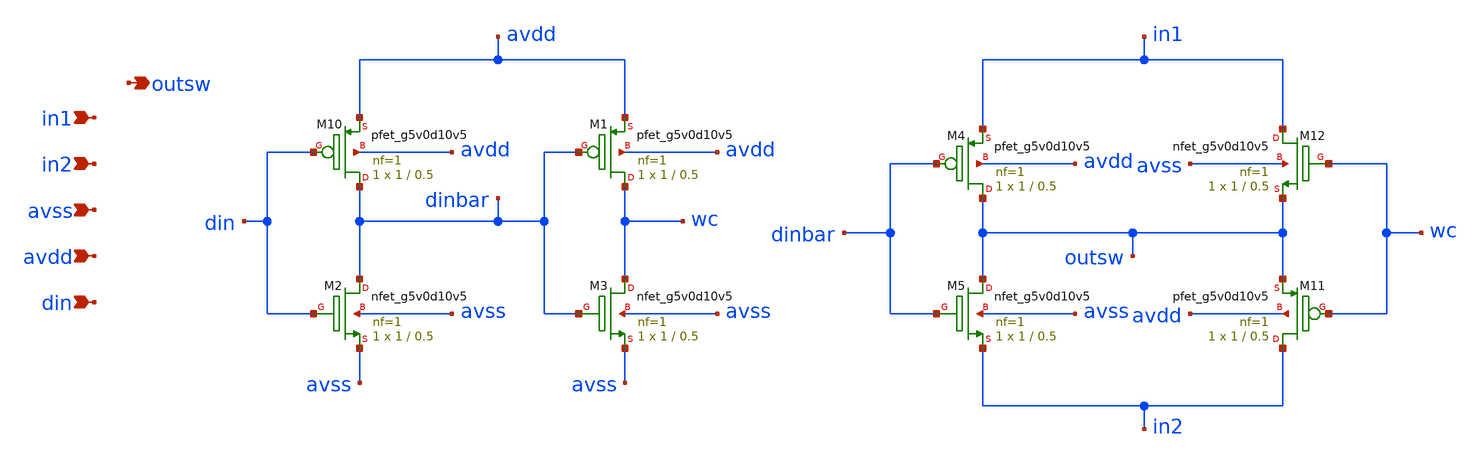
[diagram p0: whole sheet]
** sch_path: xschem/switch.sch
**.subckt switch avss avdd din in1 in2 outsw
*.ipin avss
*.ipin avdd
*.ipin din
*.ipin in1
*.ipin in2
*.opin outsw
XM10 dinbar din avdd avdd sky130_fd_pr__pfet_g5v0d10v5 L=0.5 W=1 nf=1 ad='int((1 + 1)/2) * 1 / 1 * 0.29'
+ as='int((1 + 2)/2) * 1 / 1 * 0.29' pd='2*int((1 + 1)/2) * (1 / 1 + 0.29)' ps='2*int((1 + 2)/2) * (1 / 1 + 0.29)'
+ nrd='0.29 / 1 ' nrs='0.29 / 1 ' sa=0 sb=0 sd=0 mult=1 m=1
XM2 dinbar din avss avss sky130_fd_pr__nfet_g5v0d10v5 L=0.5 W=1 nf=1 ad='int((1 + 1)/2) * 1 / 1 * 0.29'
+ as='int((1 + 2)/2) * 1 / 1 * 0.29' pd='2*int((1 + 1)/2) * (1 / 1 + 0.29)' ps='2*int((1 + 2)/2) * (1 / 1 + 0.29)'
+ nrd='0.29 / 1 ' nrs='0.29 / 1 ' sa=0 sb=0 sd=0 mult=1 m=1
XM1 wc dinbar avdd avdd sky130_fd_pr__pfet_g5v0d10v5 L=0.5 W=1 nf=1 ad='int((1 + 1)/2) * 1 / 1 * 0.29'
+ as='int((1 + 2)/2) * 1 / 1 * 0.29' pd='2*int((1 + 1)/2) * (1 / 1 + 0.29)' ps='2*int((1 + 2)/2) * (1 / 1 + 0.29)'
+ nrd='0.29 / 1 ' nrs='0.29 / 1 ' sa=0 sb=0 sd=0 mult=1 m=1
XM3 wc dinbar avss avss sky130_fd_pr__nfet_g5v0d10v5 L=0.5 W=1 nf=1 ad='int((1 + 1)/2) * 1 / 1 * 0.29'
+ as='int((1 + 2)/2) * 1 / 1 * 0.29' pd='2*int((1 + 1)/2) * (1 / 1 + 0.29)' ps='2*int((1 + 2)/2) * (1 / 1 + 0.29)'
+ nrd='0.29 / 1 ' nrs='0.29 / 1 ' sa=0 sb=0 sd=0 mult=1 m=1
XM5 outsw dinbar in2 avss sky130_fd_pr__nfet_g5v0d10v5 L=0.5 W=1 nf=1 ad='int((1 + 1)/2) * 1 / 1 * 0.29'
+ as='int((1 + 2)/2) * 1 / 1 * 0.29' pd='2*int((1 + 1)/2) * (1 / 1 + 0.29)' ps='2*int((1 + 2)/2) * (1 / 1 + 0.29)'
+ nrd='0.29 / 1 ' nrs='0.29 / 1 ' sa=0 sb=0 sd=0 mult=1 m=1
XM4 outsw dinbar in1 avdd sky130_fd_pr__pfet_g5v0d10v5 L=0.5 W=1 nf=1 ad='int((1 + 1)/2) * 1 / 1 * 0.29'
+ as='int((1 + 2)/2) * 1 / 1 * 0.29' pd='2*int((1 + 1)/2) * (1 / 1 + 0.29)' ps='2*int((1 + 2)/2) * (1 / 1 + 0.29)'
+ nrd='0.29 / 1 ' nrs='0.29 / 1 ' sa=0 sb=0 sd=0 mult=1 m=1
XM11 in2 wc outsw avdd sky130_fd_pr__pfet_g5v0d10v5 L=0.5 W=1 nf=1 ad='int((1 + 1)/2) * 1 / 1 * 0.29'
+ as='int((1 + 2)/2) * 1 / 1 * 0.29' pd='2*int((1 + 1)/2) * (1 / 1 + 0.29)' ps='2*int((1 + 2)/2) * (1 / 1 + 0.29)'
+ nrd='0.29 / 1 ' nrs='0.29 / 1 ' sa=0 sb=0 sd=0 mult=1 m=1
XM12 in1 wc outsw avss sky130_fd_pr__nfet_g5v0d10v5 L=0.5 W=1 nf=1 ad='int((1 + 1)/2) * 1 / 1 * 0.29'
+ as='int((1 + 2)/2) * 1 / 1 * 0.29' pd='2*int((1 + 1)/2) * (1 / 1 + 0.29)' ps='2*int((1 + 2)/2) * (1 / 1 + 0.29)'
+ nrd='0.29 / 1 ' nrs='0.29 / 1 ' sa=0 sb=0 sd=0 mult=1 m=1
**.ends
.end
